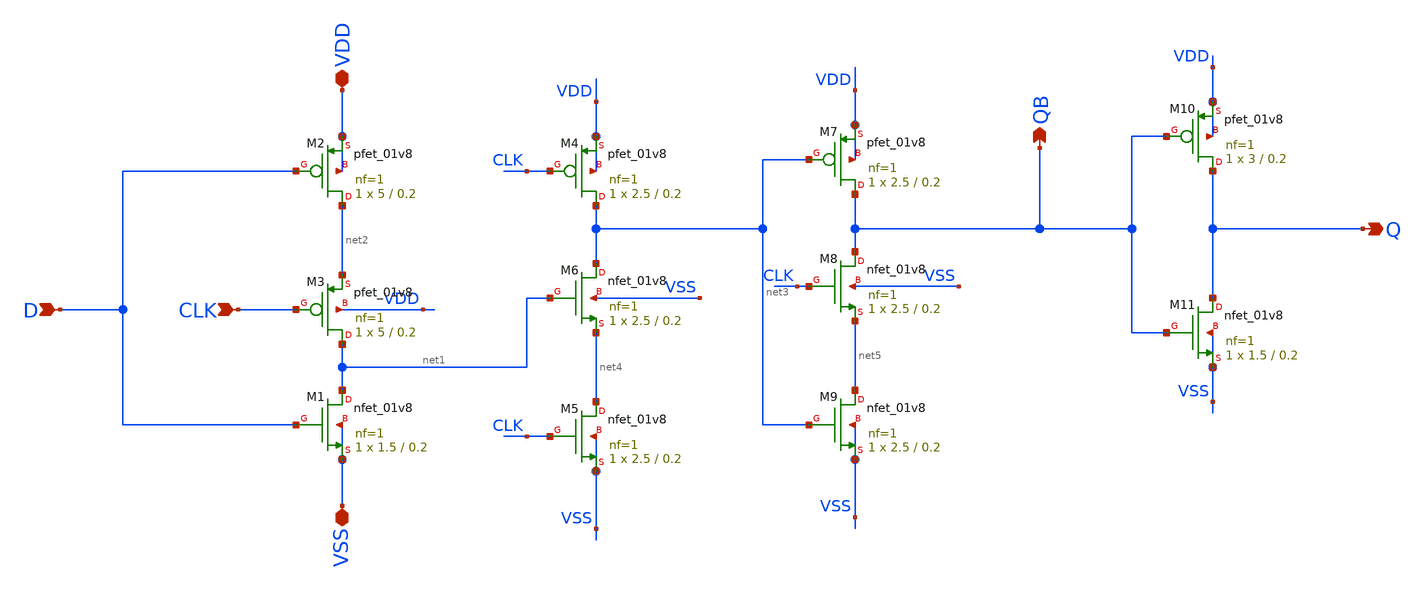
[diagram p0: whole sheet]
** sch_path: Xschem/PLL_TOP_Schematics/tspc_FF.sch
**.subckt tspc_FF D CLK VDD VSS QB Q
*.ipin D
*.ipin CLK
*.iopin VDD
*.iopin VSS
*.opin QB
*.opin Q
XM2 net2 D VDD VDD sky130_fd_pr__pfet_01v8 L=0.2 W=5 nf=1 ad='int((nf+1)/2) * W/nf * 0.29' as='int((nf+2)/2) * W/nf * 0.29'
+ pd='2*int((nf+1)/2) * (W/nf + 0.29)' ps='2*int((nf+2)/2) * (W/nf + 0.29)' nrd='0.29 / W' nrs='0.29 / W'
+ sa=0 sb=0 sd=0 mult=1 m=1
XM3 net1 CLK net2 VDD sky130_fd_pr__pfet_01v8 L=0.2 W=5 nf=1 ad='int((nf+1)/2) * W/nf * 0.29' as='int((nf+2)/2) * W/nf * 0.29'
+ pd='2*int((nf+1)/2) * (W/nf + 0.29)' ps='2*int((nf+2)/2) * (W/nf + 0.29)' nrd='0.29 / W' nrs='0.29 / W'
+ sa=0 sb=0 sd=0 mult=1 m=1
XM4 net3 CLK VDD VDD sky130_fd_pr__pfet_01v8 L=0.2 W=2.5 nf=1 ad='int((nf+1)/2) * W/nf * 0.29' as='int((nf+2)/2) * W/nf * 0.29'
+ pd='2*int((nf+1)/2) * (W/nf + 0.29)' ps='2*int((nf+2)/2) * (W/nf + 0.29)' nrd='0.29 / W' nrs='0.29 / W'
+ sa=0 sb=0 sd=0 mult=1 m=1
XM7 QB net3 VDD VDD sky130_fd_pr__pfet_01v8 L=0.2 W=2.5 nf=1 ad='int((nf+1)/2) * W/nf * 0.29' as='int((nf+2)/2) * W/nf * 0.29'
+ pd='2*int((nf+1)/2) * (W/nf + 0.29)' ps='2*int((nf+2)/2) * (W/nf + 0.29)' nrd='0.29 / W' nrs='0.29 / W'
+ sa=0 sb=0 sd=0 mult=1 m=1
XM10 Q QB VDD VDD sky130_fd_pr__pfet_01v8 L=0.2 W=3 nf=1 ad='int((nf+1)/2) * W/nf * 0.29' as='int((nf+2)/2) * W/nf * 0.29'
+ pd='2*int((nf+1)/2) * (W/nf + 0.29)' ps='2*int((nf+2)/2) * (W/nf + 0.29)' nrd='0.29 / W' nrs='0.29 / W'
+ sa=0 sb=0 sd=0 mult=1 m=1
XM1 net1 D VSS VSS sky130_fd_pr__nfet_01v8 L=0.2 W=1.5 nf=1 ad='int((nf+1)/2) * W/nf * 0.29' as='int((nf+2)/2) * W/nf * 0.29'
+ pd='2*int((nf+1)/2) * (W/nf + 0.29)' ps='2*int((nf+2)/2) * (W/nf + 0.29)' nrd='0.29 / W' nrs='0.29 / W'
+ sa=0 sb=0 sd=0 mult=1 m=1
XM5 net4 CLK VSS VSS sky130_fd_pr__nfet_01v8 L=0.2 W=2.5 nf=1 ad='int((nf+1)/2) * W/nf * 0.29' as='int((nf+2)/2) * W/nf * 0.29'
+ pd='2*int((nf+1)/2) * (W/nf + 0.29)' ps='2*int((nf+2)/2) * (W/nf + 0.29)' nrd='0.29 / W' nrs='0.29 / W'
+ sa=0 sb=0 sd=0 mult=1 m=1
XM6 net3 net1 net4 VSS sky130_fd_pr__nfet_01v8 L=0.2 W=2.5 nf=1 ad='int((nf+1)/2) * W/nf * 0.29' as='int((nf+2)/2) * W/nf * 0.29'
+ pd='2*int((nf+1)/2) * (W/nf + 0.29)' ps='2*int((nf+2)/2) * (W/nf + 0.29)' nrd='0.29 / W' nrs='0.29 / W'
+ sa=0 sb=0 sd=0 mult=1 m=1
XM8 QB CLK net5 VSS sky130_fd_pr__nfet_01v8 L=0.2 W=2.5 nf=1 ad='int((nf+1)/2) * W/nf * 0.29' as='int((nf+2)/2) * W/nf * 0.29'
+ pd='2*int((nf+1)/2) * (W/nf + 0.29)' ps='2*int((nf+2)/2) * (W/nf + 0.29)' nrd='0.29 / W' nrs='0.29 / W'
+ sa=0 sb=0 sd=0 mult=1 m=1
XM9 net5 net3 VSS VSS sky130_fd_pr__nfet_01v8 L=0.2 W=2.5 nf=1 ad='int((nf+1)/2) * W/nf * 0.29' as='int((nf+2)/2) * W/nf * 0.29'
+ pd='2*int((nf+1)/2) * (W/nf + 0.29)' ps='2*int((nf+2)/2) * (W/nf + 0.29)' nrd='0.29 / W' nrs='0.29 / W'
+ sa=0 sb=0 sd=0 mult=1 m=1
XM11 Q QB VSS VSS sky130_fd_pr__nfet_01v8 L=0.2 W=1.5 nf=1 ad='int((nf+1)/2) * W/nf * 0.29' as='int((nf+2)/2) * W/nf * 0.29'
+ pd='2*int((nf+1)/2) * (W/nf + 0.29)' ps='2*int((nf+2)/2) * (W/nf + 0.29)' nrd='0.29 / W' nrs='0.29 / W'
+ sa=0 sb=0 sd=0 mult=1 m=1
**.ends
.end
